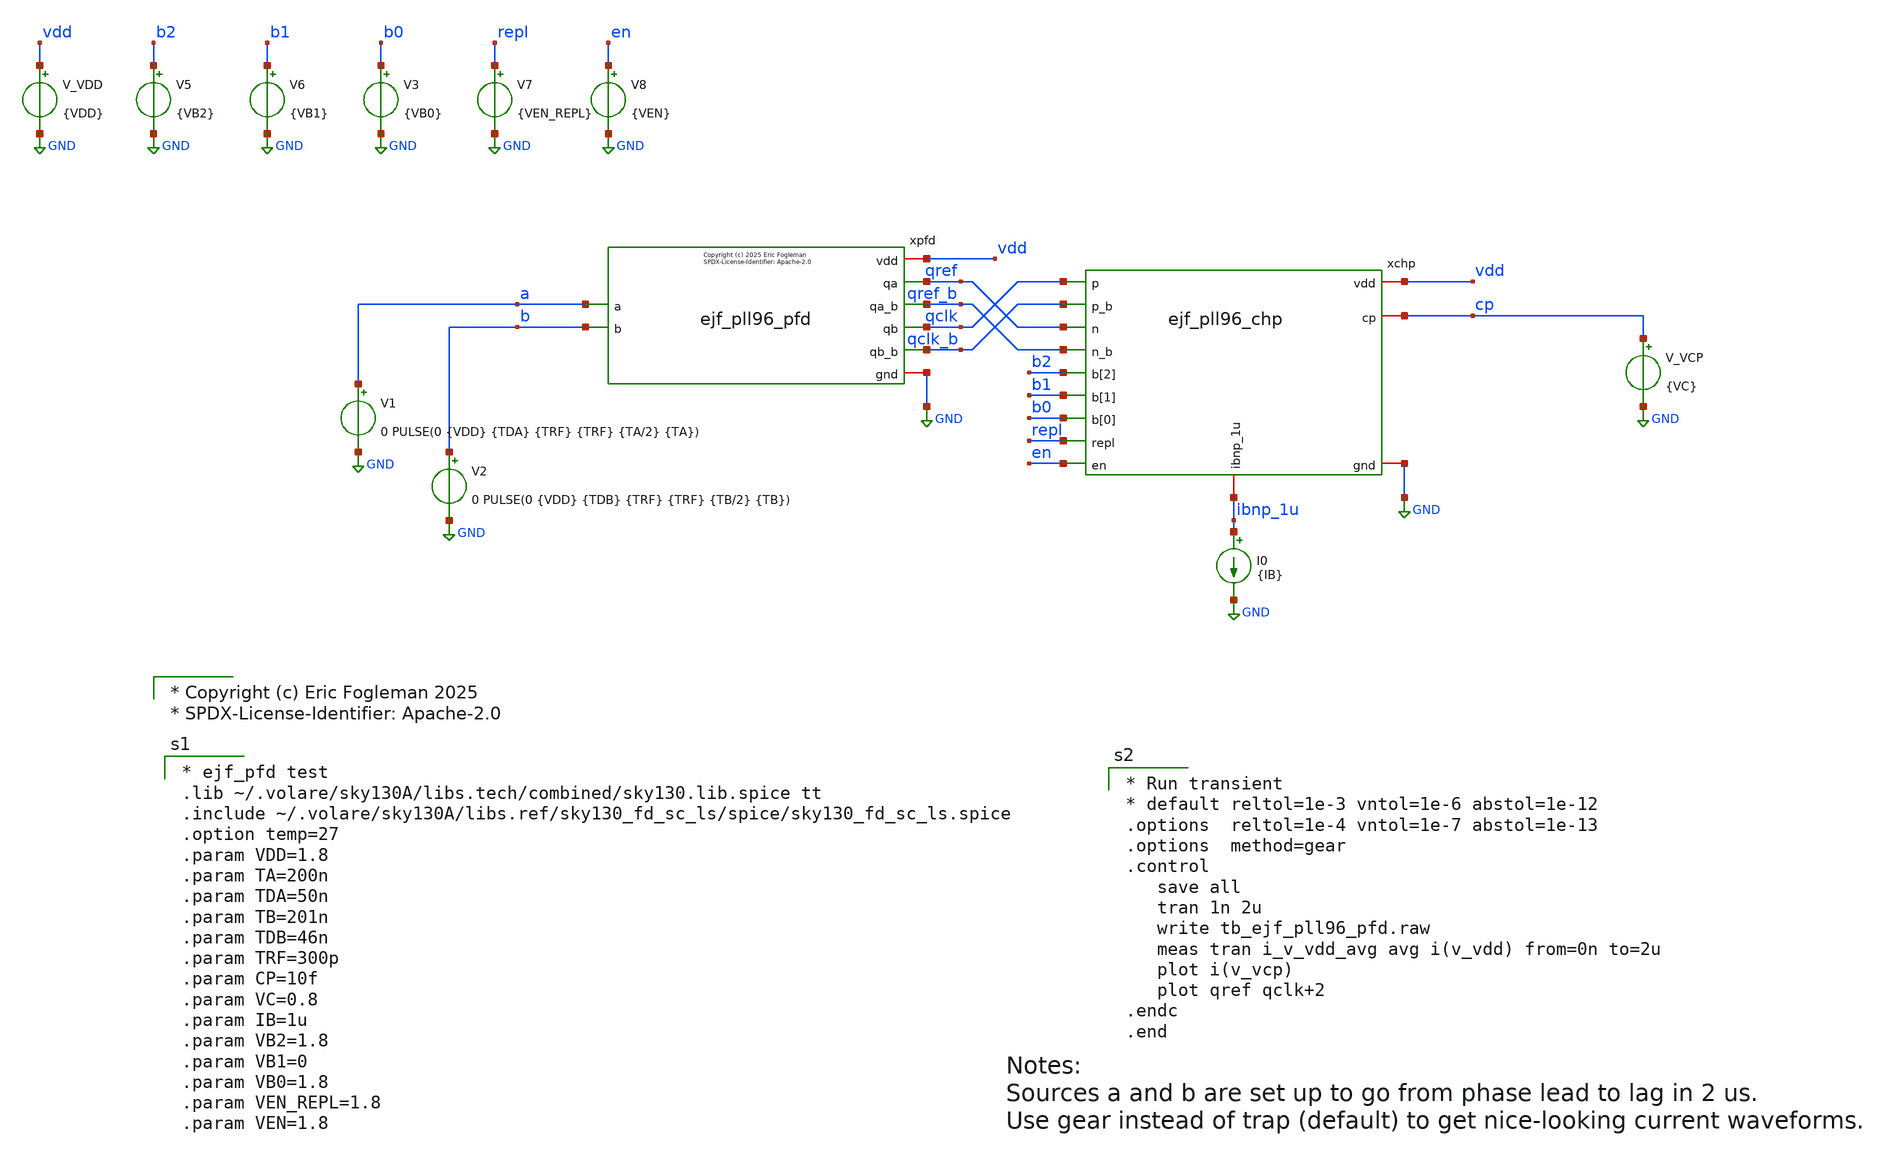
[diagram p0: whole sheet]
** sch_path: xschem/tb_ejf_pll96_pfd.sch

* Copyright (c) Eric Fogleman 2025
* SPDX-License-Identifier: Apache-2.0

**.subckt tb_ejf_pll96_pfd
V_VDD vdd GND {VDD}
.save i(v_vdd)
V1 a GND 0 PULSE(0 {VDD} {TDA} {TRF} {TRF} {TA/2} {TA})
xpfd qref a qclk b vdd GND qref_b qclk_b ejf_pll96_pfd
V2 b GND 0 PULSE(0 {VDD} {TDB} {TRF} {TRF} {TB/2} {TB})
xchp vdd qclk ibnp_1u qclk_b cp qref_b qref GND b1 repl en b2 b0 ejf_pll96_chp
I0 ibnp_1u GND {IB}
V_VCP cp GND {VC}
.save i(v_vcp)
V5 b2 GND {VB2}
.save i(v5)
V6 b1 GND {VB1}
.save i(v6)
V7 repl GND {VEN_REPL}
.save i(v7)
V8 en GND {VEN}
.save i(v8)
V3 b0 GND {VB0}
.save i(v3)
**** begin user architecture code

* ejf_pfd test
.lib ~/.volare/sky130A/libs.tech/combined/sky130.lib.spice tt
.include ~/.volare/sky130A/libs.ref/sky130_fd_sc_ls/spice/sky130_fd_sc_ls.spice
.option temp=27
.param VDD=1.8
.param TA=200n
.param TDA=50n
.param TB=201n
.param TDB=46n
.param TRF=300p
.param CP=10f
.param VC=0.8
.param IB=1u
.param VB2=1.8
.param VB1=0
.param VB0=1.8
.param VEN_REPL=1.8
.param VEN=1.8



* Run transient
* default reltol=1e-3 vntol=1e-6 abstol=1e-12
.options  reltol=1e-4 vntol=1e-7 abstol=1e-13
.options  method=gear
.control
   save all
   tran 1n 2u
   write tb_ejf_pll96_pfd.raw
   meas tran i_v_vdd_avg avg i(v_vdd) from=0n to=2u
   plot i(v_vcp)
   plot qref qclk+2
.endc
.end

**** end user architecture code
**.ends
.GLOBAL GND
.end
